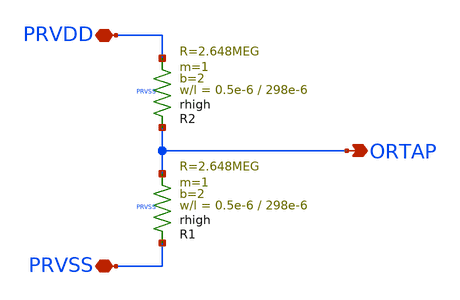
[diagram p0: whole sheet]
** sch_path: xschem/res_divider.sch
**.subckt res_divider PRVDD PRVSS ORTAP
*.iopin PRVDD
*.iopin PRVSS
*.opin ORTAP
XR1 PRVSS ORTAP PRVSS rhigh w=0.5e-6 l=298e-6 m=1 b=2 mm_ok=1
XR2 ORTAP PRVDD PRVSS rhigh w=0.5e-6 l=298e-6 m=1 b=2 mm_ok=1
**.ends
.end
